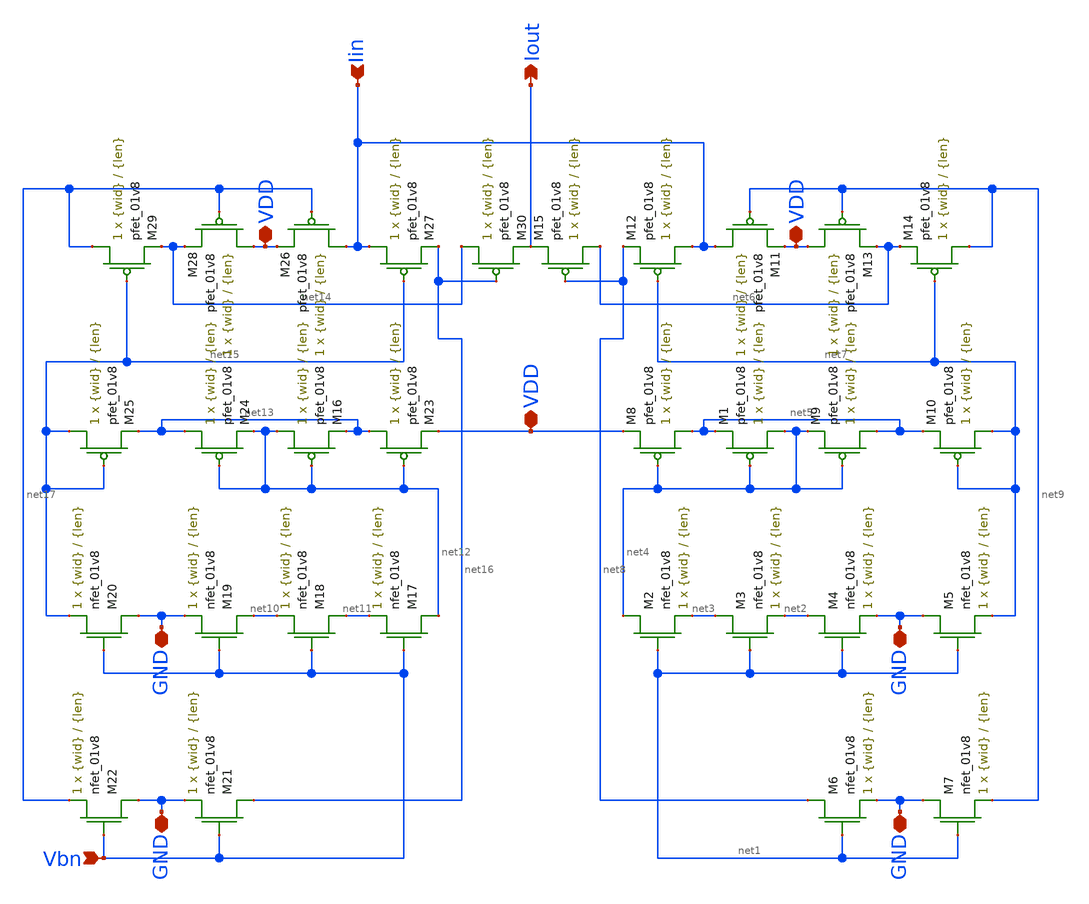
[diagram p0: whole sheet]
** sch_path: mp3/mirror_lvs.sch
**.subckt mirror_lvs Vbn Iin GND GND GND GND VDD VDD VDD Iout
*.ipin Vbn
*.ipin Iin
*.iopin GND
*.iopin GND
*.iopin GND
*.iopin GND
*.iopin VDD
*.iopin VDD
*.iopin VDD
*.opin Iout
XM1 net4 net4 net5 VDD sky130_fd_pr__pfet_01v8 L={len} W={wid} nf=1 ad='int((nf+1)/2) * W/nf * 0.29'
+ as='int((nf+2)/2) * W/nf * 0.29' pd='2*int((nf+1)/2) * (W/nf + 0.29)' ps='2*int((nf+2)/2) * (W/nf + 0.29)'
+ nrd='0.29 / W' nrs='0.29 / W' sa=0 sb=0 sd=0 mult=1 m=1
XM2 net4 net1 net3 GND sky130_fd_pr__nfet_01v8 L={len} W={wid} nf=1 ad='int((nf+1)/2) * W/nf * 0.29'
+ as='int((nf+2)/2) * W/nf * 0.29' pd='2*int((nf+1)/2) * (W/nf + 0.29)' ps='2*int((nf+2)/2) * (W/nf + 0.29)'
+ nrd='0.29 / W' nrs='0.29 / W' sa=0 sb=0 sd=0 mult=1 m=1
XM3 net3 net1 net2 GND sky130_fd_pr__nfet_01v8 L={len} W={wid} nf=1 ad='int((nf+1)/2) * W/nf * 0.29'
+ as='int((nf+2)/2) * W/nf * 0.29' pd='2*int((nf+1)/2) * (W/nf + 0.29)' ps='2*int((nf+2)/2) * (W/nf + 0.29)'
+ nrd='0.29 / W' nrs='0.29 / W' sa=0 sb=0 sd=0 mult=1 m=1
XM4 net2 net1 GND GND sky130_fd_pr__nfet_01v8 L={len} W={wid} nf=1 ad='int((nf+1)/2) * W/nf * 0.29' as='int((nf+2)/2) * W/nf * 0.29'
+ pd='2*int((nf+1)/2) * (W/nf + 0.29)' ps='2*int((nf+2)/2) * (W/nf + 0.29)' nrd='0.29 / W' nrs='0.29 / W'
+ sa=0 sb=0 sd=0 mult=1 m=1
XM5 GND net1 net7 GND sky130_fd_pr__nfet_01v8 L={len} W={wid} nf=1 ad='int((nf+1)/2) * W/nf * 0.29' as='int((nf+2)/2) * W/nf * 0.29'
+ pd='2*int((nf+1)/2) * (W/nf + 0.29)' ps='2*int((nf+2)/2) * (W/nf + 0.29)' nrd='0.29 / W' nrs='0.29 / W'
+ sa=0 sb=0 sd=0 mult=1 m=1
XM6 net8 net1 GND GND sky130_fd_pr__nfet_01v8 L={len} W={wid} nf=1 ad='int((nf+1)/2) * W/nf * 0.29' as='int((nf+2)/2) * W/nf * 0.29'
+ pd='2*int((nf+1)/2) * (W/nf + 0.29)' ps='2*int((nf+2)/2) * (W/nf + 0.29)' nrd='0.29 / W' nrs='0.29 / W'
+ sa=0 sb=0 sd=0 mult=1 m=1
XM7 GND net1 net9 GND sky130_fd_pr__nfet_01v8 L={len} W={wid} nf=1 ad='int((nf+1)/2) * W/nf * 0.29' as='int((nf+2)/2) * W/nf * 0.29'
+ pd='2*int((nf+1)/2) * (W/nf + 0.29)' ps='2*int((nf+2)/2) * (W/nf + 0.29)' nrd='0.29 / W' nrs='0.29 / W'
+ sa=0 sb=0 sd=0 mult=1 m=1
XM8 net5 net4 VDD VDD sky130_fd_pr__pfet_01v8 L={len} W={wid} nf=1 ad='int((nf+1)/2) * W/nf * 0.29' as='int((nf+2)/2) * W/nf * 0.29'
+ pd='2*int((nf+1)/2) * (W/nf + 0.29)' ps='2*int((nf+2)/2) * (W/nf + 0.29)' nrd='0.29 / W' nrs='0.29 / W'
+ sa=0 sb=0 sd=0 mult=1 m=1
XM9 net5 net4 net4 VDD sky130_fd_pr__pfet_01v8 L={len} W={wid} nf=1 ad='int((nf+1)/2) * W/nf * 0.29'
+ as='int((nf+2)/2) * W/nf * 0.29' pd='2*int((nf+1)/2) * (W/nf + 0.29)' ps='2*int((nf+2)/2) * (W/nf + 0.29)'
+ nrd='0.29 / W' nrs='0.29 / W' sa=0 sb=0 sd=0 mult=1 m=1
XM10 net7 net7 net5 VDD sky130_fd_pr__pfet_01v8 L={len} W={wid} nf=1 ad='int((nf+1)/2) * W/nf * 0.29'
+ as='int((nf+2)/2) * W/nf * 0.29' pd='2*int((nf+1)/2) * (W/nf + 0.29)' ps='2*int((nf+2)/2) * (W/nf + 0.29)'
+ nrd='0.29 / W' nrs='0.29 / W' sa=0 sb=0 sd=0 mult=1 m=1
XM11 Iin net9 VDD VDD sky130_fd_pr__pfet_01v8 L={len} W={wid} nf=1 ad='int((nf+1)/2) * W/nf * 0.29' as='int((nf+2)/2) * W/nf * 0.29'
+ pd='2*int((nf+1)/2) * (W/nf + 0.29)' ps='2*int((nf+2)/2) * (W/nf + 0.29)' nrd='0.29 / W' nrs='0.29 / W'
+ sa=0 sb=0 sd=0 mult=1 m=1
XM12 Iin net7 net8 VDD sky130_fd_pr__pfet_01v8 L={len} W={wid} nf=1 ad='int((nf+1)/2) * W/nf * 0.29'
+ as='int((nf+2)/2) * W/nf * 0.29' pd='2*int((nf+1)/2) * (W/nf + 0.29)' ps='2*int((nf+2)/2) * (W/nf + 0.29)'
+ nrd='0.29 / W' nrs='0.29 / W' sa=0 sb=0 sd=0 mult=1 m=1
XM13 VDD net9 net6 VDD sky130_fd_pr__pfet_01v8 L={len} W={wid} nf=1 ad='int((nf+1)/2) * W/nf * 0.29'
+ as='int((nf+2)/2) * W/nf * 0.29' pd='2*int((nf+1)/2) * (W/nf + 0.29)' ps='2*int((nf+2)/2) * (W/nf + 0.29)'
+ nrd='0.29 / W' nrs='0.29 / W' sa=0 sb=0 sd=0 mult=1 m=1
XM14 net9 net7 net6 VDD sky130_fd_pr__pfet_01v8 L={len} W={wid} nf=1 ad='int((nf+1)/2) * W/nf * 0.29'
+ as='int((nf+2)/2) * W/nf * 0.29' pd='2*int((nf+1)/2) * (W/nf + 0.29)' ps='2*int((nf+2)/2) * (W/nf + 0.29)'
+ nrd='0.29 / W' nrs='0.29 / W' sa=0 sb=0 sd=0 mult=1 m=1
XM15 net6 net8 Iout VDD sky130_fd_pr__pfet_01v8 L={len} W={wid} nf=1 ad='int((nf+1)/2) * W/nf * 0.29'
+ as='int((nf+2)/2) * W/nf * 0.29' pd='2*int((nf+1)/2) * (W/nf + 0.29)' ps='2*int((nf+2)/2) * (W/nf + 0.29)'
+ nrd='0.29 / W' nrs='0.29 / W' sa=0 sb=0 sd=0 mult=1 m=1
XM16 net12 net12 net13 VDD sky130_fd_pr__pfet_01v8 L={len} W={wid} nf=1 ad='int((nf+1)/2) * W/nf * 0.29'
+ as='int((nf+2)/2) * W/nf * 0.29' pd='2*int((nf+1)/2) * (W/nf + 0.29)' ps='2*int((nf+2)/2) * (W/nf + 0.29)'
+ nrd='0.29 / W' nrs='0.29 / W' sa=0 sb=0 sd=0 mult=1 m=1
XM17 net12 Vbn net11 GND sky130_fd_pr__nfet_01v8 L={len} W={wid} nf=1 ad='int((nf+1)/2) * W/nf * 0.29'
+ as='int((nf+2)/2) * W/nf * 0.29' pd='2*int((nf+1)/2) * (W/nf + 0.29)' ps='2*int((nf+2)/2) * (W/nf + 0.29)'
+ nrd='0.29 / W' nrs='0.29 / W' sa=0 sb=0 sd=0 mult=1 m=1
XM18 net11 Vbn net10 GND sky130_fd_pr__nfet_01v8 L={len} W={wid} nf=1 ad='int((nf+1)/2) * W/nf * 0.29'
+ as='int((nf+2)/2) * W/nf * 0.29' pd='2*int((nf+1)/2) * (W/nf + 0.29)' ps='2*int((nf+2)/2) * (W/nf + 0.29)'
+ nrd='0.29 / W' nrs='0.29 / W' sa=0 sb=0 sd=0 mult=1 m=1
XM19 net10 Vbn GND GND sky130_fd_pr__nfet_01v8 L={len} W={wid} nf=1 ad='int((nf+1)/2) * W/nf * 0.29'
+ as='int((nf+2)/2) * W/nf * 0.29' pd='2*int((nf+1)/2) * (W/nf + 0.29)' ps='2*int((nf+2)/2) * (W/nf + 0.29)'
+ nrd='0.29 / W' nrs='0.29 / W' sa=0 sb=0 sd=0 mult=1 m=1
XM20 GND Vbn net15 GND sky130_fd_pr__nfet_01v8 L={len} W={wid} nf=1 ad='int((nf+1)/2) * W/nf * 0.29'
+ as='int((nf+2)/2) * W/nf * 0.29' pd='2*int((nf+1)/2) * (W/nf + 0.29)' ps='2*int((nf+2)/2) * (W/nf + 0.29)'
+ nrd='0.29 / W' nrs='0.29 / W' sa=0 sb=0 sd=0 mult=1 m=1
XM21 net16 Vbn GND GND sky130_fd_pr__nfet_01v8 L={len} W={wid} nf=1 ad='int((nf+1)/2) * W/nf * 0.29'
+ as='int((nf+2)/2) * W/nf * 0.29' pd='2*int((nf+1)/2) * (W/nf + 0.29)' ps='2*int((nf+2)/2) * (W/nf + 0.29)'
+ nrd='0.29 / W' nrs='0.29 / W' sa=0 sb=0 sd=0 mult=1 m=1
XM22 GND Vbn net17 GND sky130_fd_pr__nfet_01v8 L={len} W={wid} nf=1 ad='int((nf+1)/2) * W/nf * 0.29'
+ as='int((nf+2)/2) * W/nf * 0.29' pd='2*int((nf+1)/2) * (W/nf + 0.29)' ps='2*int((nf+2)/2) * (W/nf + 0.29)'
+ nrd='0.29 / W' nrs='0.29 / W' sa=0 sb=0 sd=0 mult=1 m=1
XM23 net13 net12 VDD VDD sky130_fd_pr__pfet_01v8 L={len} W={wid} nf=1 ad='int((nf+1)/2) * W/nf * 0.29'
+ as='int((nf+2)/2) * W/nf * 0.29' pd='2*int((nf+1)/2) * (W/nf + 0.29)' ps='2*int((nf+2)/2) * (W/nf + 0.29)'
+ nrd='0.29 / W' nrs='0.29 / W' sa=0 sb=0 sd=0 mult=1 m=1
XM24 net13 net12 net12 VDD sky130_fd_pr__pfet_01v8 L={len} W={wid} nf=1 ad='int((nf+1)/2) * W/nf * 0.29'
+ as='int((nf+2)/2) * W/nf * 0.29' pd='2*int((nf+1)/2) * (W/nf + 0.29)' ps='2*int((nf+2)/2) * (W/nf + 0.29)'
+ nrd='0.29 / W' nrs='0.29 / W' sa=0 sb=0 sd=0 mult=1 m=1
XM25 net15 net15 net13 VDD sky130_fd_pr__pfet_01v8 L={len} W={wid} nf=1 ad='int((nf+1)/2) * W/nf * 0.29'
+ as='int((nf+2)/2) * W/nf * 0.29' pd='2*int((nf+1)/2) * (W/nf + 0.29)' ps='2*int((nf+2)/2) * (W/nf + 0.29)'
+ nrd='0.29 / W' nrs='0.29 / W' sa=0 sb=0 sd=0 mult=1 m=1
XM26 Iin net17 VDD VDD sky130_fd_pr__pfet_01v8 L={len} W={wid} nf=1 ad='int((nf+1)/2) * W/nf * 0.29'
+ as='int((nf+2)/2) * W/nf * 0.29' pd='2*int((nf+1)/2) * (W/nf + 0.29)' ps='2*int((nf+2)/2) * (W/nf + 0.29)'
+ nrd='0.29 / W' nrs='0.29 / W' sa=0 sb=0 sd=0 mult=1 m=1
XM27 Iin net15 net16 VDD sky130_fd_pr__pfet_01v8 L={len} W={wid} nf=1 ad='int((nf+1)/2) * W/nf * 0.29'
+ as='int((nf+2)/2) * W/nf * 0.29' pd='2*int((nf+1)/2) * (W/nf + 0.29)' ps='2*int((nf+2)/2) * (W/nf + 0.29)'
+ nrd='0.29 / W' nrs='0.29 / W' sa=0 sb=0 sd=0 mult=1 m=1
XM28 VDD net17 net14 VDD sky130_fd_pr__pfet_01v8 L={len} W={wid} nf=1 ad='int((nf+1)/2) * W/nf * 0.29'
+ as='int((nf+2)/2) * W/nf * 0.29' pd='2*int((nf+1)/2) * (W/nf + 0.29)' ps='2*int((nf+2)/2) * (W/nf + 0.29)'
+ nrd='0.29 / W' nrs='0.29 / W' sa=0 sb=0 sd=0 mult=1 m=1
XM29 net17 net15 net14 VDD sky130_fd_pr__pfet_01v8 L={len} W={wid} nf=1 ad='int((nf+1)/2) * W/nf * 0.29'
+ as='int((nf+2)/2) * W/nf * 0.29' pd='2*int((nf+1)/2) * (W/nf + 0.29)' ps='2*int((nf+2)/2) * (W/nf + 0.29)'
+ nrd='0.29 / W' nrs='0.29 / W' sa=0 sb=0 sd=0 mult=1 m=1
XM30 net14 net16 Iout VDD sky130_fd_pr__pfet_01v8 L={len} W={wid} nf=1 ad='int((nf+1)/2) * W/nf * 0.29'
+ as='int((nf+2)/2) * W/nf * 0.29' pd='2*int((nf+1)/2) * (W/nf + 0.29)' ps='2*int((nf+2)/2) * (W/nf + 0.29)'
+ nrd='0.29 / W' nrs='0.29 / W' sa=0 sb=0 sd=0 mult=1 m=1
**.ends
.end
